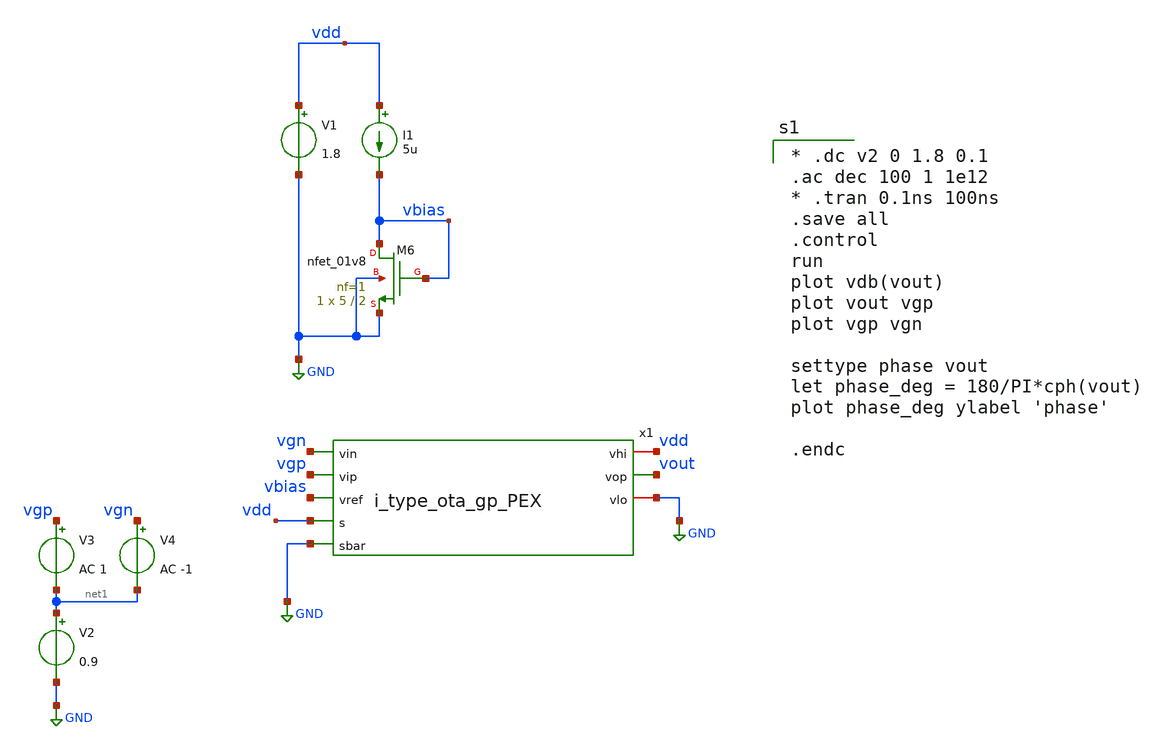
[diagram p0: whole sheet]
** sch_path: xschem/i_type_ota_actb1.sch
**.subckt i_type_ota_actb1
XM6 vbias vbias GND GND sky130_fd_pr__nfet_01v8 L=2 W=5 nf=1 ad='int((nf+1)/2) * W/nf * 0.29' as='int((nf+2)/2) * W/nf * 0.29'
+ pd='2*int((nf+1)/2) * (W/nf + 0.29)' ps='2*int((nf+2)/2) * (W/nf + 0.29)' nrd='0.29 / W' nrs='0.29 / W'
+ sa=0 sb=0 sd=0 mult=1 m=1
I1 vdd vbias 5u
V1 vdd GND 1.8
V2 net1 GND 0.9
V3 vgp net1 AC 1
x1 vdd vout vgn vgp vbias vdd GND GND i_type_ota_gp_PEX
V4 vgn net1 AC -1
**** begin user architecture code
.lib $::SKYWATER_MODELS/sky130.lib.spice tt
.include $::PDKPATH/libs.ref/sky130_fd_sc_hs/spice/sky130_fd_sc_hs.spice


* .dc v2 0 1.8 0.1
.ac dec 100 1 1e12
* .tran 0.1ns 100ns
.save all
.control
run
plot vdb(vout)
plot vout vgp
plot vgp vgn

settype phase vout
let phase_deg = 180/PI*cph(vout)
plot phase_deg ylabel 'phase'

.endc


**** end user architecture code
**.ends

* expanding   symbol:  i_type_ota_gp_PEX.sym # of pins=8
** sym_path: xschem/i_type_ota_gp_PEX.sym
** sch_path: xschem/i_type_ota_gp_PEX.sch
.subckt i_type_ota_gp_PEX vhi vop vin vip vref s sbar vlo
*.ipin vip
*.ipin vin
*.opin vop
*.iopin vhi
*.iopin vlo
*.ipin vref
*.ipin s
*.ipin sbar
**** begin user architecture code

* NGSPICE file created from cmota_1_flat.ext - technology: sky130A

.subckt cmota_gp VHI VLO VREF VIP VIN VOP S SBAR

* NGSPICE file created from cmota_gp_flat.ext - technology: sky130A

X0 VHI a_n210_n3012# VOP VHI sky130_fd_pr__pfet_01v8 ad=0p pd=0u as=0p ps=0u w=1e+07u l=300000u
X1 a_n2570_n3012# VIN a_n1037_n4100# VLO sky130_fd_pr__nfet_01v8_lvt ad=0p pd=0u as=0p ps=0u
+ w=2.5e+06u l=150000u
X2 a_n1037_n4100# VIP a_n210_n3012# VLO sky130_fd_pr__nfet_01v8_lvt ad=0p pd=0u as=0p ps=0u
+ w=2.5e+06u l=150000u
X3 VOP a_n210_n3012# VHI VHI sky130_fd_pr__pfet_01v8 ad=0p pd=0u as=0p ps=0u w=1e+07u l=300000u
X4 VHI a_n210_n3012# VOP VHI sky130_fd_pr__pfet_01v8 ad=0p pd=0u as=0p ps=0u w=1e+07u l=300000u
X5 VOP a_n210_n3012# VHI VHI sky130_fd_pr__pfet_01v8 ad=0p pd=0u as=0p ps=0u w=1e+07u l=300000u
X6 VREF a_n4194_n6504# VLO sky130_fd_pr__res_xhigh_po w=350000u l=1.49e+06u
X7 a_2927_n3812# VOP sky130_fd_pr__cap_mim_m3_2 l=1.8e+07u w=7e+06u
X8 VOP a_n2689_n5512# VLO VLO sky130_fd_pr__nfet_01v8 ad=0p pd=0u as=0p ps=0u w=1e+07u l=300000u
X9 VLO VLO a_n1037_n4100# VLO sky130_fd_pr__nfet_01v8_lvt ad=0p pd=0u as=0p ps=0u w=2.5e+06u
+ l=150000u
X10 VHI a_n210_n3012# VOP VHI sky130_fd_pr__pfet_01v8 ad=0p pd=0u as=0p ps=0u w=1e+07u l=300000u
X11 a_n2689_n5512# a_n2570_n3012# VHI VHI sky130_fd_pr__pfet_01v8 ad=0p pd=0u as=0p ps=0u w=1e+07u
+ l=300000u
X12 VLO a_n2689_n5512# VOP VLO sky130_fd_pr__nfet_01v8 ad=0p pd=0u as=0p ps=0u w=1e+07u l=300000u
X13 VLO a_n4150_n6044# a_n1037_n4100# VLO sky130_fd_pr__nfet_01v8 ad=0p pd=0u as=0p ps=0u w=1e+07u
+ l=2e+06u
X14 VHI VHI VHI VHI sky130_fd_pr__pfet_01v8 ad=0p pd=0u as=0p ps=0u w=1e+07u l=300000u
X15 VLO VLO VLO VLO sky130_fd_pr__nfet_01v8 ad=0p pd=0u as=0p ps=0u w=1e+07u l=300000u
X16 a_n2689_n5512# a_n2689_n5512# VLO VLO sky130_fd_pr__nfet_01v8 ad=0p pd=0u as=0p ps=0u w=1e+07u
+ l=300000u
X17 VHI VHI VHI VHI sky130_fd_pr__pfet_01v8 ad=0p pd=0u as=0p ps=0u w=1e+07u l=300000u
X18 VHI VHI VHI VHI sky130_fd_pr__pfet_01v8 ad=0p pd=0u as=0p ps=0u w=1e+07u l=300000u
X19 a_n210_n3012# VIP a_n1037_n4100# VLO sky130_fd_pr__nfet_01v8_lvt ad=0p pd=0u as=0p ps=0u
+ w=2.5e+06u l=150000u
X20 VLO a_n2689_n5512# a_n2689_n5512# VLO sky130_fd_pr__nfet_01v8 ad=0p pd=0u as=0p ps=0u w=1e+07u
+ l=300000u
X21 a_n2689_n5512# a_n2570_n3012# VHI VHI sky130_fd_pr__pfet_01v8 ad=0p pd=0u as=0p ps=0u w=1e+07u
+ l=300000u
X22 VLO a_n2689_n5512# VOP VLO sky130_fd_pr__nfet_01v8 ad=0p pd=0u as=0p ps=0u w=1e+07u l=300000u
X23 a_n2689_n5512# a_n2570_n3012# VHI VHI sky130_fd_pr__pfet_01v8 ad=0p pd=0u as=0p ps=0u w=1e+07u
+ l=300000u
X24 VHI a_n2570_n3012# a_n2689_n5512# VHI sky130_fd_pr__pfet_01v8 ad=0p pd=0u as=0p ps=0u w=1e+07u
+ l=300000u
X25 VOP a_n210_n3012# VHI VHI sky130_fd_pr__pfet_01v8 ad=0p pd=0u as=0p ps=0u w=1e+07u l=300000u
X26 VHI a_n2570_n3012# a_n2689_n5512# VHI sky130_fd_pr__pfet_01v8 ad=0p pd=0u as=0p ps=0u w=1e+07u
+ l=300000u
X27 VLO VLO VLO VLO sky130_fd_pr__nfet_01v8_lvt ad=0p pd=0u as=0p ps=0u w=2.5e+06u l=150000u
X28 a_n2689_n5512# a_n2570_n3012# VHI VHI sky130_fd_pr__pfet_01v8 ad=0p pd=0u as=0p ps=0u w=1e+07u
+ l=300000u
X29 VHI VLO sky130_fd_pr__cap_mim_m3_1 l=3.1e+07u w=1.3e+07u
X30 VHI a_n210_n3012# a_n210_n3012# VHI sky130_fd_pr__pfet_01v8 ad=0p pd=0u as=0p ps=0u w=1e+07u
+ l=300000u
X31 a_n2570_n3012# VIN a_n1037_n4100# VLO sky130_fd_pr__nfet_01v8_lvt ad=0p pd=0u as=0p ps=0u
+ w=2.5e+06u l=150000u
X32 a_n1037_n4100# VLO VLO VLO sky130_fd_pr__nfet_01v8_lvt ad=0p pd=0u as=0p ps=0u w=2.5e+06u
+ l=150000u
X33 VOP a_n210_n3012# VHI VHI sky130_fd_pr__pfet_01v8 ad=0p pd=0u as=0p ps=0u w=1e+07u l=300000u
X34 a_n4150_n6044# S a_n4194_n6504# VLO sky130_fd_pr__nfet_01v8 ad=0p pd=0u as=0p ps=0u w=2.5e+06u
+ l=150000u
X35 VHI a_n210_n3012# VOP VHI sky130_fd_pr__pfet_01v8 ad=0p pd=0u as=0p ps=0u w=1e+07u l=300000u
X36 a_n4194_n6504# SBAR VLO VLO sky130_fd_pr__nfet_01v8 ad=0p pd=0u as=0p ps=0u w=2.5e+06u l=150000u
X37 VHI a_n210_n3012# a_n210_n3012# VHI sky130_fd_pr__pfet_01v8 ad=0p pd=0u as=0p ps=0u w=1e+07u
+ l=300000u
X38 a_n1037_n4100# VIN a_n2570_n3012# VLO sky130_fd_pr__nfet_01v8_lvt ad=0p pd=0u as=0p ps=0u
+ w=2.5e+06u l=150000u
X39 VLO VHI sky130_fd_pr__cap_mim_m3_2 l=3.1e+07u w=1.3e+07u
X40 VLO VLO VLO VLO sky130_fd_pr__nfet_01v8_lvt ad=0p pd=0u as=0p ps=0u w=2.5e+06u l=150000u
X41 a_n1037_n4100# VIP a_n210_n3012# VLO sky130_fd_pr__nfet_01v8_lvt ad=0p pd=0u as=0p ps=0u
+ w=2.5e+06u l=150000u
X42 a_n2689_n5512# a_n2689_n5512# VLO VLO sky130_fd_pr__nfet_01v8 ad=0p pd=0u as=0p ps=0u w=1e+07u
+ l=300000u
X43 VLO VLO VLO VLO sky130_fd_pr__nfet_01v8 ad=0p pd=0u as=0p ps=0u w=1e+07u l=300000u
X44 VLO a_n2689_n5512# a_n2689_n5512# VLO sky130_fd_pr__nfet_01v8 ad=0p pd=0u as=0p ps=0u w=1e+07u
+ l=300000u
X45 a_n210_n3012# a_n210_n3012# VHI VHI sky130_fd_pr__pfet_01v8 ad=0p pd=0u as=0p ps=0u w=1e+07u
+ l=300000u
X46 VHI a_n2570_n3012# a_n2689_n5512# VHI sky130_fd_pr__pfet_01v8 ad=0p pd=0u as=0p ps=0u w=1e+07u
+ l=300000u
X47 VOP a_n210_n3012# VHI VHI sky130_fd_pr__pfet_01v8 ad=0p pd=0u as=0p ps=0u w=1e+07u l=300000u
X48 VHI a_n2570_n3012# a_n2689_n5512# VHI sky130_fd_pr__pfet_01v8 ad=0p pd=0u as=0p ps=0u w=1e+07u
+ l=300000u
X49 VOP a_n2689_n5512# VLO VLO sky130_fd_pr__nfet_01v8 ad=0p pd=0u as=0p ps=0u w=1e+07u l=300000u
X50 a_n2689_n5512# a_n2689_n5512# VLO VLO sky130_fd_pr__nfet_01v8 ad=0p pd=0u as=0p ps=0u w=1e+07u
+ l=300000u
X51 VHI a_n2570_n3012# a_n2570_n3012# VHI sky130_fd_pr__pfet_01v8 ad=0p pd=0u as=0p ps=0u w=1e+07u
+ l=300000u
X52 a_n2689_n5512# a_n2570_n3012# VHI VHI sky130_fd_pr__pfet_01v8 ad=0p pd=0u as=0p ps=0u w=1e+07u
+ l=300000u
X53 a_n2689_n5512# a_n2570_n3012# VHI VHI sky130_fd_pr__pfet_01v8 ad=0p pd=0u as=0p ps=0u w=1e+07u
+ l=300000u
X54 VLO a_n2689_n5512# VOP VLO sky130_fd_pr__nfet_01v8 ad=0p pd=0u as=0p ps=0u w=1e+07u l=300000u
X55 VHI a_n210_n3012# VOP VHI sky130_fd_pr__pfet_01v8 ad=0p pd=0u as=0p ps=0u w=1e+07u l=300000u
X56 a_n2570_n3012# a_n2570_n3012# VHI VHI sky130_fd_pr__pfet_01v8 ad=0p pd=0u as=0p ps=0u w=1e+07u
+ l=300000u
X57 VOP a_n210_n3012# VHI VHI sky130_fd_pr__pfet_01v8 ad=0p pd=0u as=0p ps=0u w=1e+07u l=300000u
X58 VOP a_n2689_n5512# VLO VLO sky130_fd_pr__nfet_01v8 ad=0p pd=0u as=0p ps=0u w=1e+07u l=300000u
X59 VHI a_n2570_n3012# a_n2570_n3012# VHI sky130_fd_pr__pfet_01v8 ad=0p pd=0u as=0p ps=0u w=1e+07u
+ l=300000u
X60 a_n1037_n4100# VIP a_n210_n3012# VLO sky130_fd_pr__nfet_01v8_lvt ad=0p pd=0u as=0p ps=0u
+ w=2.5e+06u l=150000u
X61 a_n210_n3012# VIP a_n1037_n4100# VLO sky130_fd_pr__nfet_01v8_lvt ad=0p pd=0u as=0p ps=0u
+ w=2.5e+06u l=150000u
X62 VHI a_n210_n3012# VOP VHI sky130_fd_pr__pfet_01v8 ad=0p pd=0u as=0p ps=0u w=1e+07u l=300000u
X63 VLO a_n2689_n5512# VOP VLO sky130_fd_pr__nfet_01v8 ad=0p pd=0u as=0p ps=0u w=1e+07u l=300000u
X64 VOP a_n210_n3012# VHI VHI sky130_fd_pr__pfet_01v8 ad=0p pd=0u as=0p ps=0u w=1e+07u l=300000u
X65 VLO a_n4150_n6044# sky130_fd_pr__cap_mim_m3_1 l=2.7e+07u w=5.5e+06u
X66 VLO VLO VLO VLO sky130_fd_pr__nfet_01v8 ad=0p pd=0u as=0p ps=0u w=1e+07u l=300000u
X67 a_n2689_n5512# a_2927_n3812# VLO sky130_fd_pr__res_high_po w=690000u l=3.43e+06u
X68 VLO a_n4150_n6044# a_n1037_n4100# VLO sky130_fd_pr__nfet_01v8 ad=0p pd=0u as=0p ps=0u w=1e+07u
+ l=2e+06u
X69 a_n1037_n4100# VIP a_n210_n3012# VLO sky130_fd_pr__nfet_01v8_lvt ad=0p pd=0u as=0p ps=0u
+ w=2.5e+06u l=150000u
X70 a_n210_n3012# a_n210_n3012# VHI VHI sky130_fd_pr__pfet_01v8 ad=0p pd=0u as=0p ps=0u w=1e+07u
+ l=300000u
X71 a_n210_n3012# VIP a_n1037_n4100# VLO sky130_fd_pr__nfet_01v8_lvt ad=0p pd=0u as=0p ps=0u
+ w=2.5e+06u l=150000u
X72 VOP a_n210_n3012# VHI VHI sky130_fd_pr__pfet_01v8 ad=0p pd=0u as=0p ps=0u w=1e+07u l=300000u
X73 a_n1037_n4100# a_n4150_n6044# VLO VLO sky130_fd_pr__nfet_01v8 ad=0p pd=0u as=0p ps=0u w=1e+07u
+ l=2e+06u
X74 VLO SBAR a_n4194_n6504# VLO sky130_fd_pr__nfet_01v8 ad=0p pd=0u as=0p ps=0u w=2.5e+06u l=150000u
X75 a_n210_n3012# VIP a_n1037_n4100# VLO sky130_fd_pr__nfet_01v8_lvt ad=0p pd=0u as=0p ps=0u
+ w=2.5e+06u l=150000u
X76 a_n1037_n4100# VIN a_n2570_n3012# VLO sky130_fd_pr__nfet_01v8_lvt ad=0p pd=0u as=0p ps=0u
+ w=2.5e+06u l=150000u
X77 VHI a_n2570_n3012# a_n2689_n5512# VHI sky130_fd_pr__pfet_01v8 ad=0p pd=0u as=0p ps=0u w=1e+07u
+ l=300000u
X78 a_n4150_n6044# VLO sky130_fd_pr__cap_mim_m3_2 l=2.7e+07u w=5.5e+06u
X79 a_n2570_n3012# VIN a_n1037_n4100# VLO sky130_fd_pr__nfet_01v8_lvt ad=0p pd=0u as=0p ps=0u
+ w=2.5e+06u l=150000u
X80 a_n2689_n5512# a_n2570_n3012# VHI VHI sky130_fd_pr__pfet_01v8 ad=0p pd=0u as=0p ps=0u w=1e+07u
+ l=300000u
X81 VLO a_n2689_n5512# a_n2689_n5512# VLO sky130_fd_pr__nfet_01v8 ad=0p pd=0u as=0p ps=0u w=1e+07u
+ l=300000u
X82 VHI VHI VHI VHI sky130_fd_pr__pfet_01v8 ad=0p pd=0u as=0p ps=0u w=1e+07u l=300000u
X83 a_n2570_n3012# a_n2570_n3012# VHI VHI sky130_fd_pr__pfet_01v8 ad=0p pd=0u as=0p ps=0u w=1e+07u
+ l=300000u
X84 VOP a_n2689_n5512# VLO VLO sky130_fd_pr__nfet_01v8 ad=0p pd=0u as=0p ps=0u w=1e+07u l=300000u
X85 VHI a_n2570_n3012# a_n2689_n5512# VHI sky130_fd_pr__pfet_01v8 ad=0p pd=0u as=0p ps=0u w=1e+07u
+ l=300000u
X86 a_n1037_n4100# a_n4150_n6044# VLO VLO sky130_fd_pr__nfet_01v8 ad=0p pd=0u as=0p ps=0u w=1e+07u
+ l=2e+06u
X87 VHI a_n210_n3012# VOP VHI sky130_fd_pr__pfet_01v8 ad=0p pd=0u as=0p ps=0u w=1e+07u l=300000u
X88 a_n2570_n3012# VIN a_n1037_n4100# VLO sky130_fd_pr__nfet_01v8_lvt ad=0p pd=0u as=0p ps=0u
+ w=2.5e+06u l=150000u
X89 VLO VLO VLO VLO sky130_fd_pr__nfet_01v8 ad=0p pd=0u as=0p ps=0u w=1e+07u l=300000u
X90 VLO a_n2689_n5512# a_n2689_n5512# VLO sky130_fd_pr__nfet_01v8 ad=0p pd=0u as=0p ps=0u w=1e+07u
+ l=300000u
X91 VHI a_n2570_n3012# a_n2689_n5512# VHI sky130_fd_pr__pfet_01v8 ad=0p pd=0u as=0p ps=0u w=1e+07u
+ l=300000u
X92 VOP a_2927_n3812# sky130_fd_pr__cap_mim_m3_1 l=1.8e+07u w=7e+06u
X93 VHI a_n210_n3012# VOP VHI sky130_fd_pr__pfet_01v8 ad=0p pd=0u as=0p ps=0u w=1e+07u l=300000u
X94 a_n1037_n4100# VIN a_n2570_n3012# VLO sky130_fd_pr__nfet_01v8_lvt ad=0p pd=0u as=0p ps=0u
+ w=2.5e+06u l=150000u
X95 a_n2689_n5512# a_n2689_n5512# VLO VLO sky130_fd_pr__nfet_01v8 ad=0p pd=0u as=0p ps=0u w=1e+07u
+ l=300000u
X96 a_n2689_n5512# a_n2570_n3012# VHI VHI sky130_fd_pr__pfet_01v8 ad=0p pd=0u as=0p ps=0u w=1e+07u
+ l=300000u
X97 VHI a_n2570_n3012# a_n2689_n5512# VHI sky130_fd_pr__pfet_01v8 ad=0p pd=0u as=0p ps=0u w=1e+07u
+ l=300000u
X98 a_n1037_n4100# VIN a_n2570_n3012# VLO sky130_fd_pr__nfet_01v8_lvt ad=0p pd=0u as=0p ps=0u
+ w=2.5e+06u l=150000u
X99 a_n4194_n6504# S a_n4150_n6044# VLO sky130_fd_pr__nfet_01v8 ad=0p pd=0u as=0p ps=0u w=2.5e+06u
+ l=150000u
C0 a_2927_n3812# VOP 24.13fF
C1 a_n1037_n4100# a_n210_n3012# 5.97fF
C2 VHI VOP 36.36fF
C3 a_n2689_n5512# a_n2570_n3012# 2.27fF
C4 a_n2570_n3012# a_n1037_n4100# 5.98fF
C5 VHI a_n210_n3012# 14.16fF
C6 a_n4150_n6044# a_n2689_n5512# 2.39fF
C7 VHI a_n2570_n3012# 14.24fF
C8 a_n4150_n6044# a_n1037_n4100# 2.52fF
C9 a_n2689_n5512# VHI 35.73fF
C10 a_n4150_n6044# VHI 5.41fF
C11 a_2927_n3812# VHI 2.94fF
C12 a_2927_n3812# VLO 5.99fF $ **FLOATING
C13 a_n4150_n6044# VLO 50.00fF $ **FLOATING
C14 a_n1037_n4100# VLO 6.12fF $ **FLOATING
C15 VOP VLO 18.37fF $ **FLOATING
C16 a_n2689_n5512# VLO 25.04fF $ **FLOATING
C17 VHI VLO 125.94fF $ **FLOATING


.ends







XDUT vhi vlo vref vip vin vop s sbar cmota_gp


**** end user architecture code
.ends

.GLOBAL GND
.end
